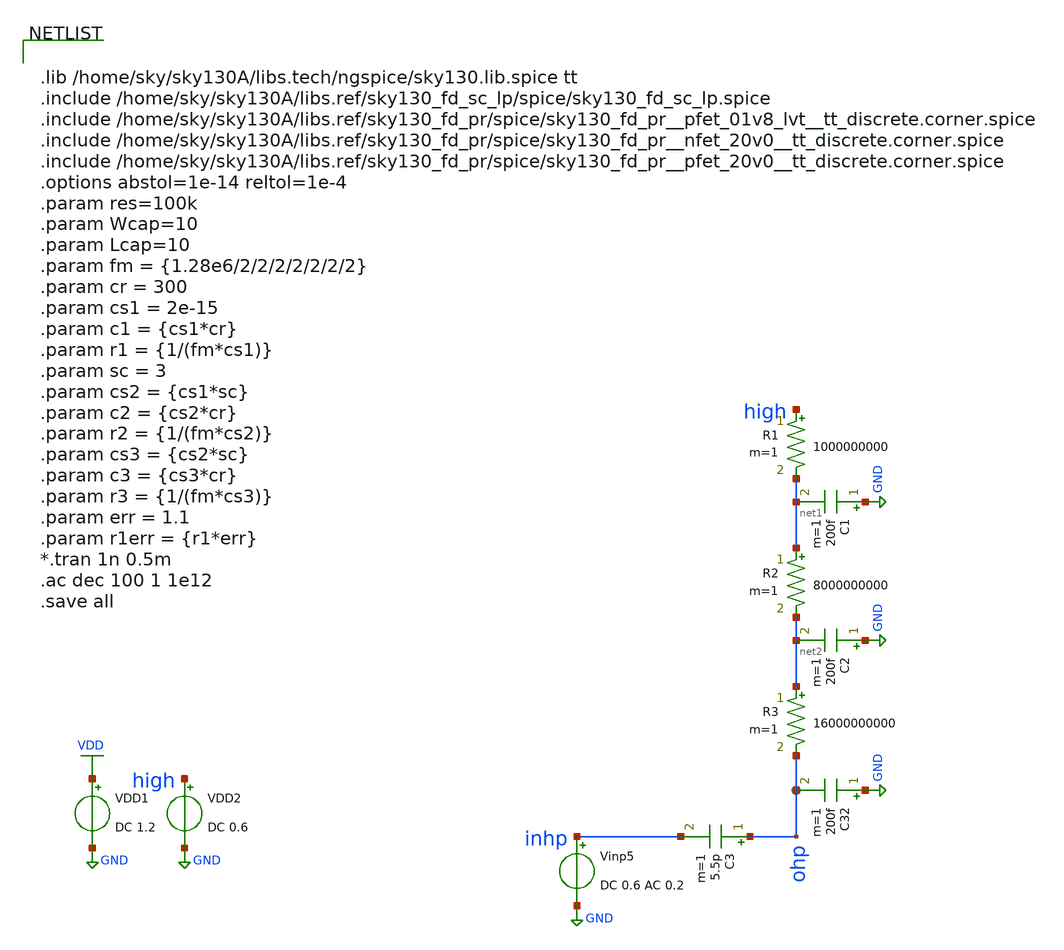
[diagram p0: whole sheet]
** sch_path: xschem/tryandtest/RCcharacterization.sch
**.subckt RCcharacterization
VDD1 VDD GND DC 1.2
C32 GND ohp 200f m=1
Vinp5 inhp GND DC 0.6 AC 0.2
R1 high net1 1000000000 m=1
R2 net1 net2 8000000000 m=1
R3 net2 ohp 16000000000 m=1
C1 GND net1 200f m=1
C2 GND net2 200f m=1
VDD2 high GND DC 0.6
C3 ohp inhp 5.5p m=1
**** begin user architecture code


.lib /home/sky/sky130A/libs.tech/ngspice/sky130.lib.spice tt
.include /home/sky/sky130A/libs.ref/sky130_fd_sc_lp/spice/sky130_fd_sc_lp.spice
.include /home/sky/sky130A/libs.ref/sky130_fd_pr/spice/sky130_fd_pr__pfet_01v8_lvt__tt_discrete.corner.spice
.include /home/sky/sky130A/libs.ref/sky130_fd_pr/spice/sky130_fd_pr__nfet_20v0__tt_discrete.corner.spice
.include /home/sky/sky130A/libs.ref/sky130_fd_pr/spice/sky130_fd_pr__pfet_20v0__tt_discrete.corner.spice
.options abstol=1e-14 reltol=1e-4
.param res=100k
.param Wcap=10
.param Lcap=10
.param fm = {1.28e6/2/2/2/2/2/2/2}
.param cr = 300
.param cs1 = 2e-15
.param c1 = {cs1*cr}
.param r1 = {1/(fm*cs1)}
.param sc = 3
.param cs2 = {cs1*sc}
.param c2 = {cs2*cr}
.param r2 = {1/(fm*cs2)}
.param cs3 = {cs2*sc}
.param c3 = {cs3*cr}
.param r3 = {1/(fm*cs3)}
.param err = 1.1
.param r1err = {r1*err}
*.tran 1n 0.5m
.ac dec 100 1 1e12
.save all


**** end user architecture code
**.ends
.GLOBAL GND
.GLOBAL VDD
.end
